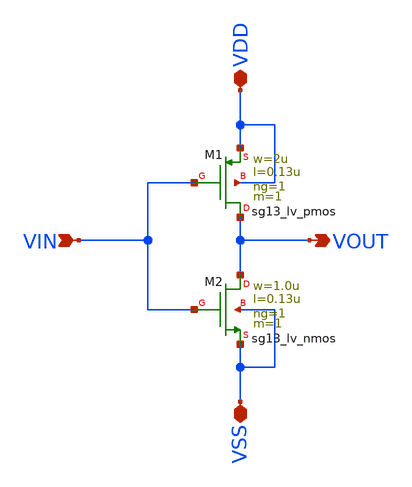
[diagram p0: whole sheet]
** sch_path: xschem/Manual_Instrucciones/simbolos/Simbolo_Support_1.sch
**.subckt Simbolo_Support_1 VIN VDD VSS VOUT
*.ipin VIN
*.iopin VDD
*.iopin VSS
*.opin VOUT
XM1 VOUT VIN VDD VDD sg13_lv_pmos w=2u l=0.13u ng=1 m=1 mm_ok=1
XM2 VOUT VIN VSS VSS sg13_lv_nmos w=1.0u l=0.13u ng=1 m=1 mm_ok=1
**.ends
.end
